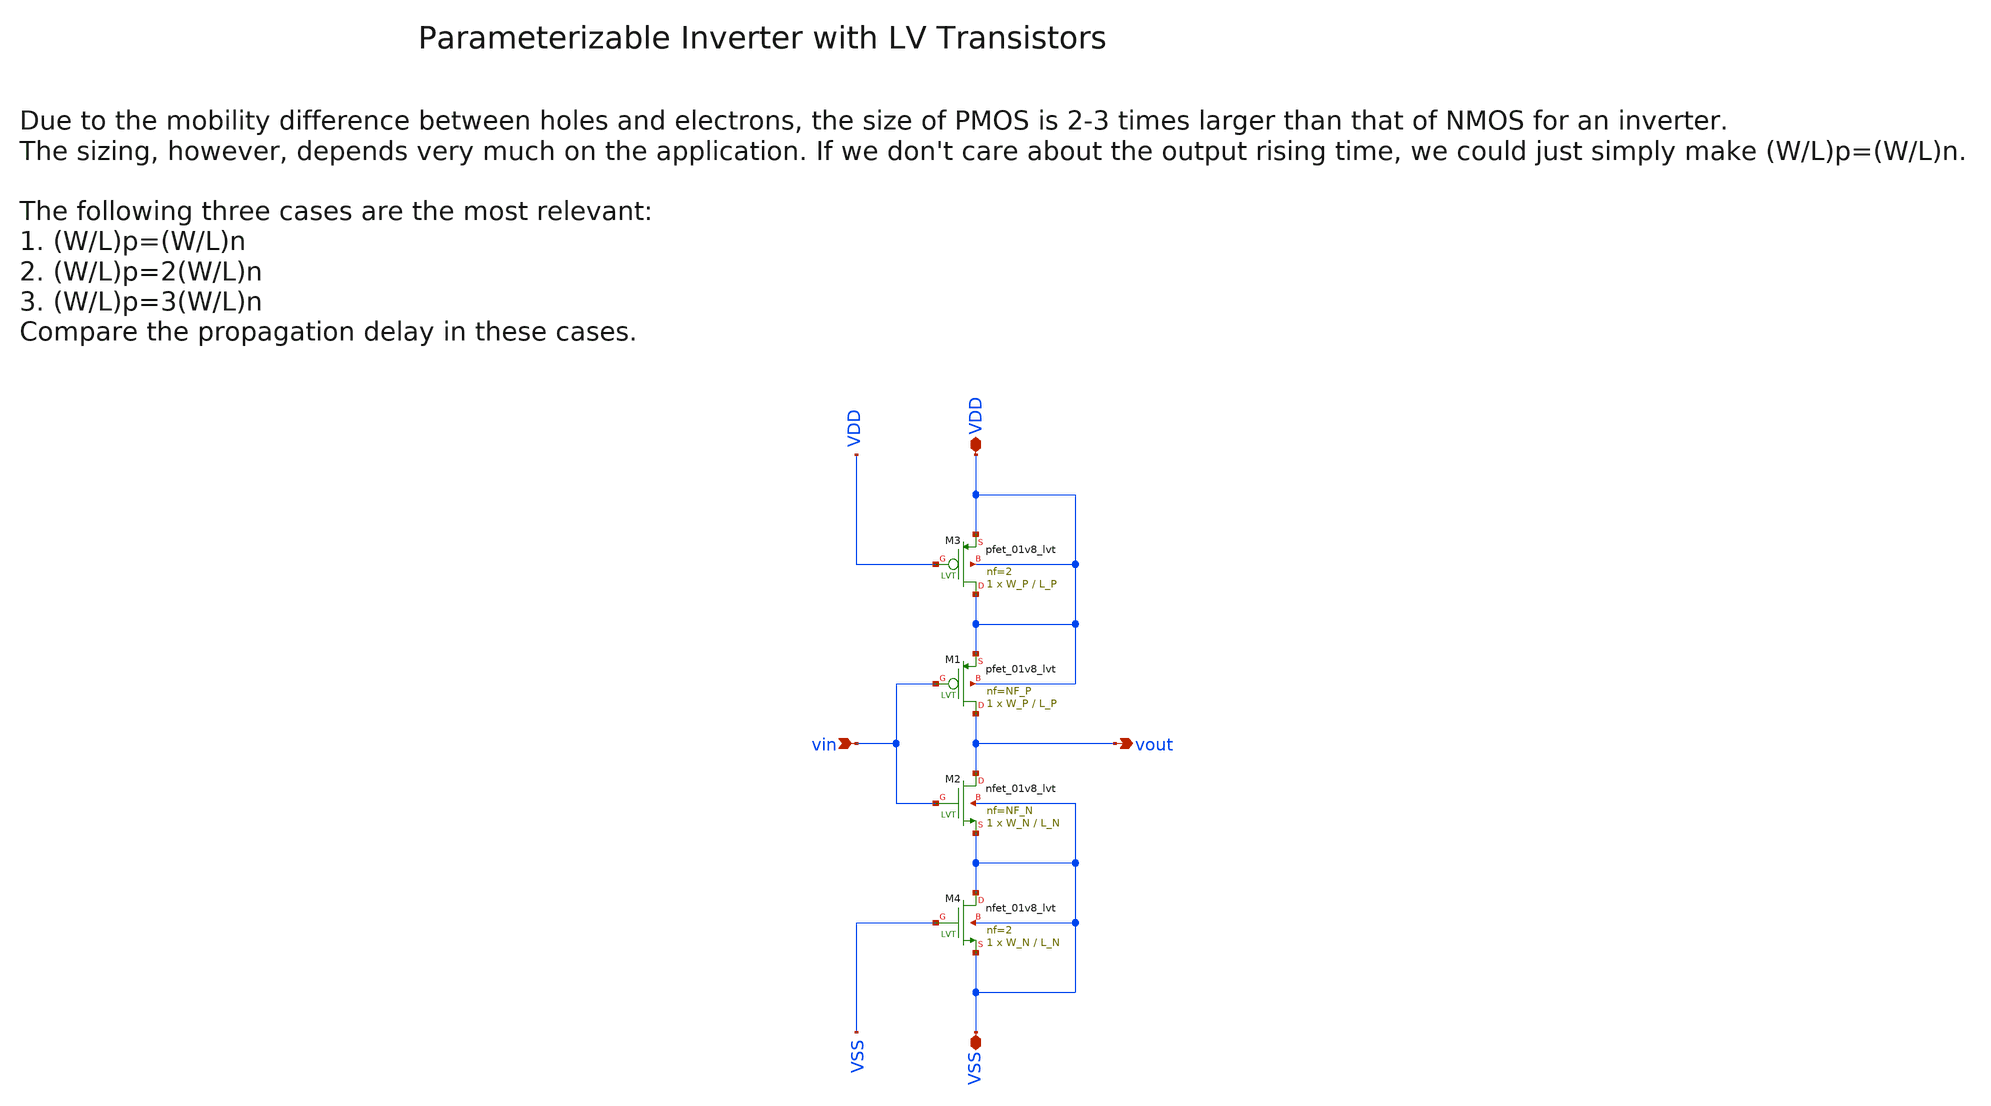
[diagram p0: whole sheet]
** sch_path: sky130/macros/iqmod/schematic/generic/wspr_tx_iqmod_mfb_lpf_ota_core_inv_lv_gen.sch
**.subckt wspr_tx_iqmod_mfb_lpf_ota_core_inv_lv_gen vin VDD VSS vout
*.ipin vin
*.iopin VDD
*.iopin VSS
*.opin vout
XM1 vout vin VDD VDD sky130_fd_pr__pfet_01v8_lvt L=L_P W=W_P nf=NF_P ad='int((NF_P + 1)/2) * W_P / NF_P * 0.29'
+ as='int((NF_P + 2)/2) * W_P / NF_P * 0.29' pd='2*int((NF_P + 1)/2) * (W_P / NF_P + 0.29)' ps='2*int((NF_P + 2)/2) * (W_P / NF_P + 0.29)'
+ nrd='0.29 / W_P ' nrs='0.29 / W_P ' sa=0 sb=0 sd=0 mult=1 m=1
XM3 VDD VDD VDD VDD sky130_fd_pr__pfet_01v8_lvt L=L_P W=W_P nf=2 ad='int((2 + 1)/2) * W_P / 2 * 0.29'
+ as='int((2 + 2)/2) * W_P / 2 * 0.29' pd='2*int((2 + 1)/2) * (W_P / 2 + 0.29)' ps='2*int((2 + 2)/2) * (W_P / 2 + 0.29)'
+ nrd='0.29 / W_P ' nrs='0.29 / W_P ' sa=0 sb=0 sd=0 mult=1 m=1
XM2 vout vin VSS VSS sky130_fd_pr__nfet_01v8_lvt L=L_N W=W_N nf=NF_N ad='int((NF_N + 1)/2) * W_N / NF_N * 0.29'
+ as='int((NF_N + 2)/2) * W_N / NF_N * 0.29' pd='2*int((NF_N + 1)/2) * (W_N / NF_N + 0.29)' ps='2*int((NF_N + 2)/2) * (W_N / NF_N + 0.29)'
+ nrd='0.29 / W_N ' nrs='0.29 / W_N ' sa=0 sb=0 sd=0 mult=1 m=1
XM4 VSS VSS VSS VSS sky130_fd_pr__nfet_01v8_lvt L=L_N W=W_N nf=2 ad='int((2 + 1)/2) * W_N / 2 * 0.29'
+ as='int((2 + 2)/2) * W_N / 2 * 0.29' pd='2*int((2 + 1)/2) * (W_N / 2 + 0.29)' ps='2*int((2 + 2)/2) * (W_N / 2 + 0.29)'
+ nrd='0.29 / W_N ' nrs='0.29 / W_N ' sa=0 sb=0 sd=0 mult=1 m=1
**.ends
.end
